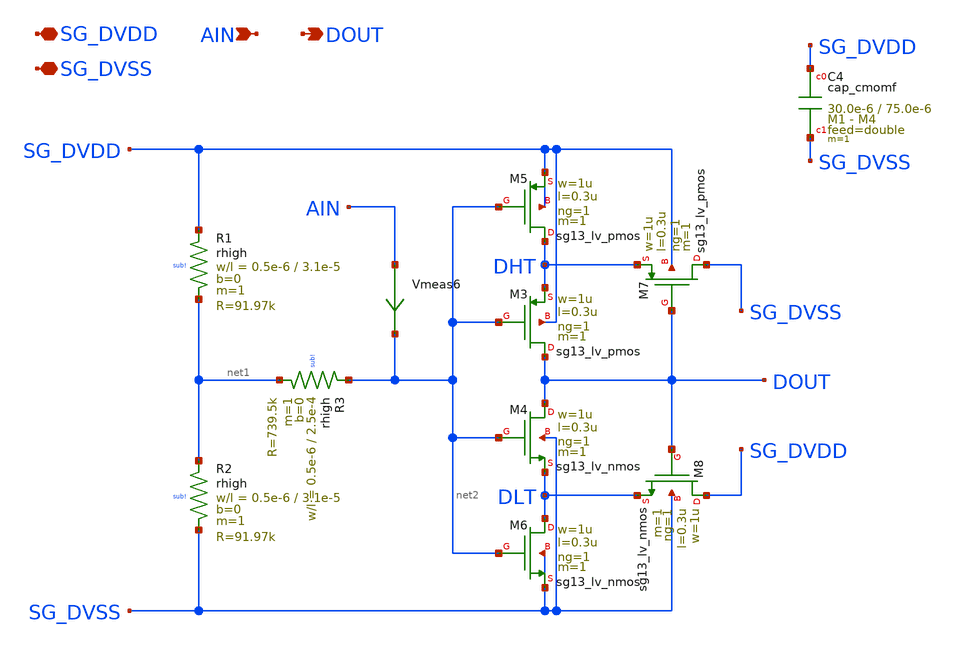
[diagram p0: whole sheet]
** sch_path: xschem/schmitt_trigger_pullmid.sch
**.subckt schmitt_trigger_pullmid SG_DVDD SG_DVSS AIN DOUT
*.iopin SG_DVDD
*.iopin SG_DVSS
*.ipin AIN
*.opin DOUT
Vmeas6 AIN net2 0
.save i(vmeas6)
XR1 SG_DVDD net1 sub! rhigh w=0.5e-6 l=3.1e-5 m=1 b=0 mm_ok=1
XR2 net1 SG_DVSS sub! rhigh w=0.5e-6 l=3.1e-5 m=1 b=0 mm_ok=1
XR3 net2 net1 sub! rhigh w=0.5e-6 l=2.5e-4 m=1 b=0 mm_ok=1
XC4 SG_DVDD SG_DVSS cap_cmomf w=30.0e-6 l=75.0e-6 mmin=1 mmax=4 feed=double subblock=0 m=1 mm_ok=1
XM4 DOUT net2 DLT SG_DVSS sg13_lv_nmos w=1u l=0.3u ng=1 m=1 mm_ok=1
XM5 DHT net2 SG_DVDD SG_DVDD sg13_lv_pmos w=1u l=0.3u ng=1 m=1 mm_ok=1
XM3 DOUT net2 DHT SG_DVDD sg13_lv_pmos w=1u l=0.3u ng=1 m=1 mm_ok=1
XM7 SG_DVSS DOUT DHT SG_DVDD sg13_lv_pmos w=1u l=0.3u ng=1 m=1 mm_ok=1
XM6 DLT net2 SG_DVSS SG_DVSS sg13_lv_nmos w=1u l=0.3u ng=1 m=1 mm_ok=1
XM8 SG_DVDD DOUT DLT SG_DVSS sg13_lv_nmos w=1u l=0.3u ng=1 m=1 mm_ok=1
**.ends
.end
